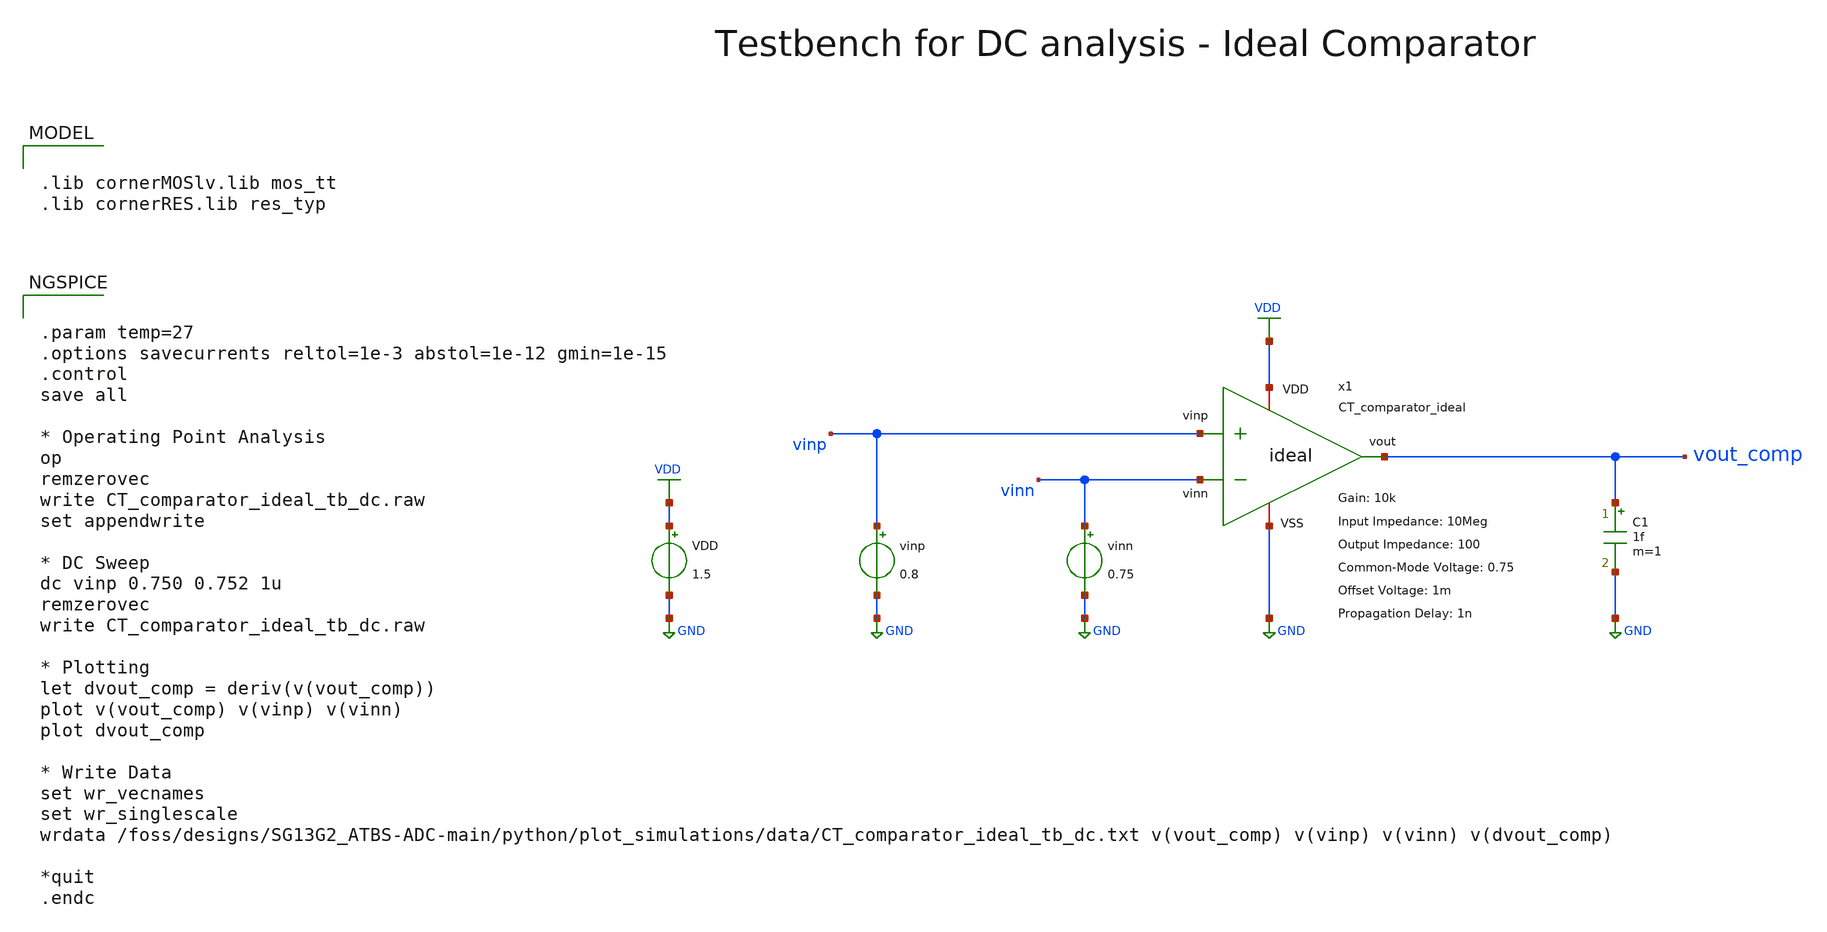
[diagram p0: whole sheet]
** sch_path: SG13G2_ATBS-ADC-main/xschem/comparator/continuous_time/ideal/testbenches/CT_comparator_ideal_tb_dc.sch
**.subckt CT_comparator_ideal_tb_dc
VDD VDD GND 1.5
C1 vout_comp GND 1f m=1
vinp vinp GND 0.8
vinn vinn GND 0.75
x1 vinp vinn VDD vout_comp GND CT_comparator_ideal A=10k Rin=10Meg Rout=100 Pdc= Vcm=0.75 Voffs=1m
+ tpd=1n
**** begin user architecture code


.param temp=27
.options savecurrents reltol=1e-3 abstol=1e-12 gmin=1e-15
.control
save all

* Operating Point Analysis
op
remzerovec
write CT_comparator_ideal_tb_dc.raw
set appendwrite

* DC Sweep
dc vinp 0.750 0.752 1u
remzerovec
write CT_comparator_ideal_tb_dc.raw

* Plotting
let dvout_comp = deriv(v(vout_comp))
plot v(vout_comp) v(vinp) v(vinn)
plot dvout_comp

* Write Data
set wr_vecnames
set wr_singlescale
wrdata /foss/designs/SG13G2_ATBS-ADC-main/python/plot_simulations/data/CT_comparator_ideal_tb_dc.txt
+ v(vout_comp) v(vinp) v(vinn) v(dvout_comp)

*quit
.endc


.lib cornerMOSlv.lib mos_tt
.lib cornerRES.lib res_typ

**** end user architecture code
**.ends

* expanding   symbol:  comparator/continuous_time/ideal/CT_comparator_ideal.sym # of pins=5
** sym_path: SG13G2_ATBS-ADC-main/xschem/comparator/continuous_time/ideal/CT_comparator_ideal.sym
** sch_path: SG13G2_ATBS-ADC-main/xschem/comparator/continuous_time/ideal/CT_comparator_ideal.sch
.subckt CT_comparator_ideal vinp vinn VDD vout VSS  A=10k Rin=10Meg Rout=100 Vcm=0.75 Voffs=1m
+ tpd=1n
*.ipin vinn
*.opin vout
*.ipin vinp
*.iopin VSS
*.iopin VDD
R1 vinp vinn {Rin} m=1
B1 net1 VSS v=v(VDD)/2*tanh({A}/(v(VDD)/2)*(v(vinp)-v(vinn)-{Voffs}))+{Vcm}
R3 net2 vout {Rout} m=1
A1 net1 net2 VSS del_subckt
.model del_subckt delay(delay=tpd buffer_size=8192)
.ends

.GLOBAL GND
.GLOBAL VDD
.end
